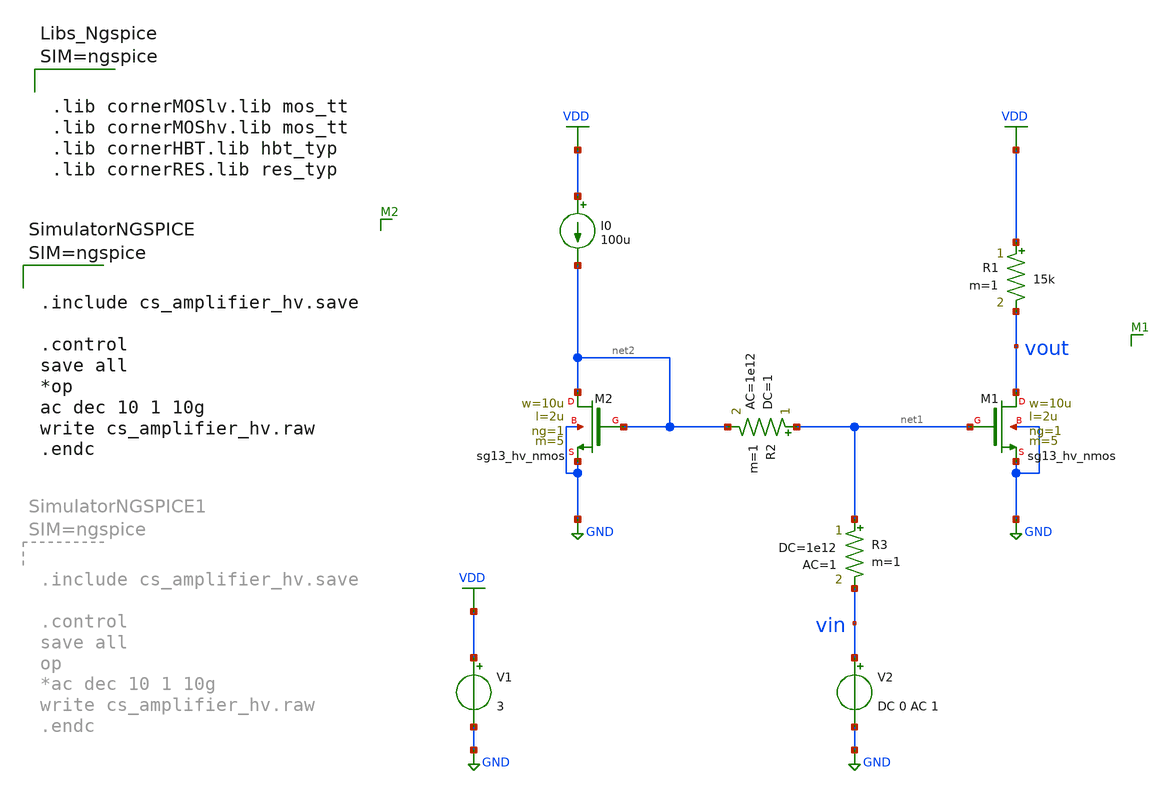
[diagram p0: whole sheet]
** sch_path: Schematics/lab_1/cs_amplifier_hv.sch
**.subckt cs_amplifier_hv
R1 VDD vout 15k m=1
I0 VDD net2 100u
R2 net1 net2 1 ac=1e12 m=1
R3 net1 vin 1e12 ac=1 m=1
V1 VDD GND 3
V2 vin GND DC 0 AC 1
XM1 vout net1 GND GND sg13_hv_nmos w=10u l=2u ng=1 m=5 mm_ok=1
XM2 net2 net2 GND GND sg13_hv_nmos w=10u l=2u ng=1 m=5 mm_ok=1
**** begin user architecture code



.lib cornerMOSlv.lib mos_tt
.lib cornerMOShv.lib mos_tt
.lib cornerHBT.lib hbt_typ
.lib cornerRES.lib res_typ






.include cs_amplifier_hv.save

.control
save all
*op
ac dec 10 1 10g
write cs_amplifier_hv.raw
.endc



**** end user architecture code
**.ends
.GLOBAL GND
.GLOBAL VDD
.end
